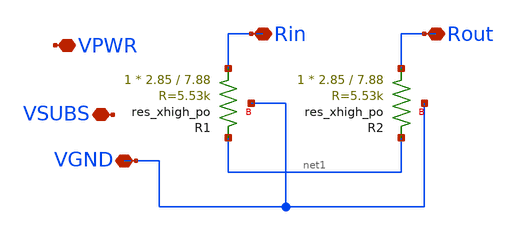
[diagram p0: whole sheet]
** sch_path: xschem/multiple_bgr/sky130_asc_res_xhigh_po_2p85_1.sch
**.subckt sky130_asc_res_xhigh_po_2p85_1 Rin Rout VPWR VGND VSUBS
*.iopin Rin
*.iopin Rout
*.iopin VPWR
*.iopin VGND
*.iopin VSUBS
XR1 Rin net1 VGND sky130_fd_pr__res_xhigh_po W=2.85 L=7.88 mult=1 m=1
XR2 Rout net1 VGND sky130_fd_pr__res_xhigh_po W=2.85 L=7.88 mult=1 m=1
**.ends
.end
